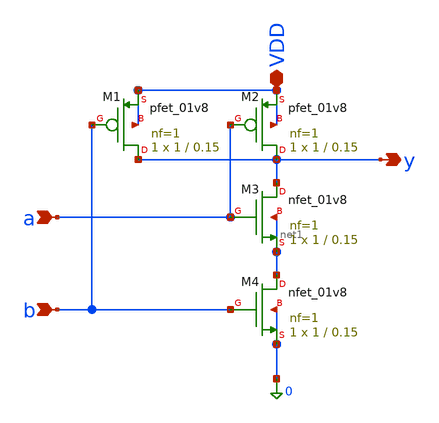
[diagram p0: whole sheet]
** sch_path: nand_gate/nand.sch
**.subckt nand a b y VDD
*.ipin a
*.ipin b
*.opin y
*.iopin VDD
XM1 y b VDD VDD sky130_fd_pr__pfet_01v8 L=0.15 W=1 nf=1 ad='int((1 + 1)/2) * 1 / 1 * 0.29' as='int((1 + 2)/2) * 1 / 1 * 0.29'
+ pd='2*int((1 + 1)/2) * (1 / 1 + 0.29)' ps='2*int((1 + 2)/2) * (1 / 1 + 0.29)' nrd='0.29 / 1 ' nrs='0.29 / 1 '
+ sa=0 sb=0 sd=0 mult=1 m=1
XM2 y a VDD VDD sky130_fd_pr__pfet_01v8 L=0.15 W=1 nf=1 ad='int((1 + 1)/2) * 1 / 1 * 0.29' as='int((1 + 2)/2) * 1 / 1 * 0.29'
+ pd='2*int((1 + 1)/2) * (1 / 1 + 0.29)' ps='2*int((1 + 2)/2) * (1 / 1 + 0.29)' nrd='0.29 / 1 ' nrs='0.29 / 1 '
+ sa=0 sb=0 sd=0 mult=1 m=1
XM3 y a net1 net1 sky130_fd_pr__nfet_01v8 L=0.15 W=1 nf=1 ad='int((1 + 1)/2) * 1 / 1 * 0.29' as='int((1 + 2)/2) * 1 / 1 * 0.29'
+ pd='2*int((1 + 1)/2) * (1 / 1 + 0.29)' ps='2*int((1 + 2)/2) * (1 / 1 + 0.29)' nrd='0.29 / 1 ' nrs='0.29 / 1 '
+ sa=0 sb=0 sd=0 mult=1 m=1
XM4 net1 b 0 0 sky130_fd_pr__nfet_01v8 L=0.15 W=1 nf=1 ad='int((1 + 1)/2) * 1 / 1 * 0.29' as='int((1 + 2)/2) * 1 / 1 * 0.29'
+ pd='2*int((1 + 1)/2) * (1 / 1 + 0.29)' ps='2*int((1 + 2)/2) * (1 / 1 + 0.29)' nrd='0.29 / 1 ' nrs='0.29 / 1 '
+ sa=0 sb=0 sd=0 mult=1 m=1
**.ends
.end
